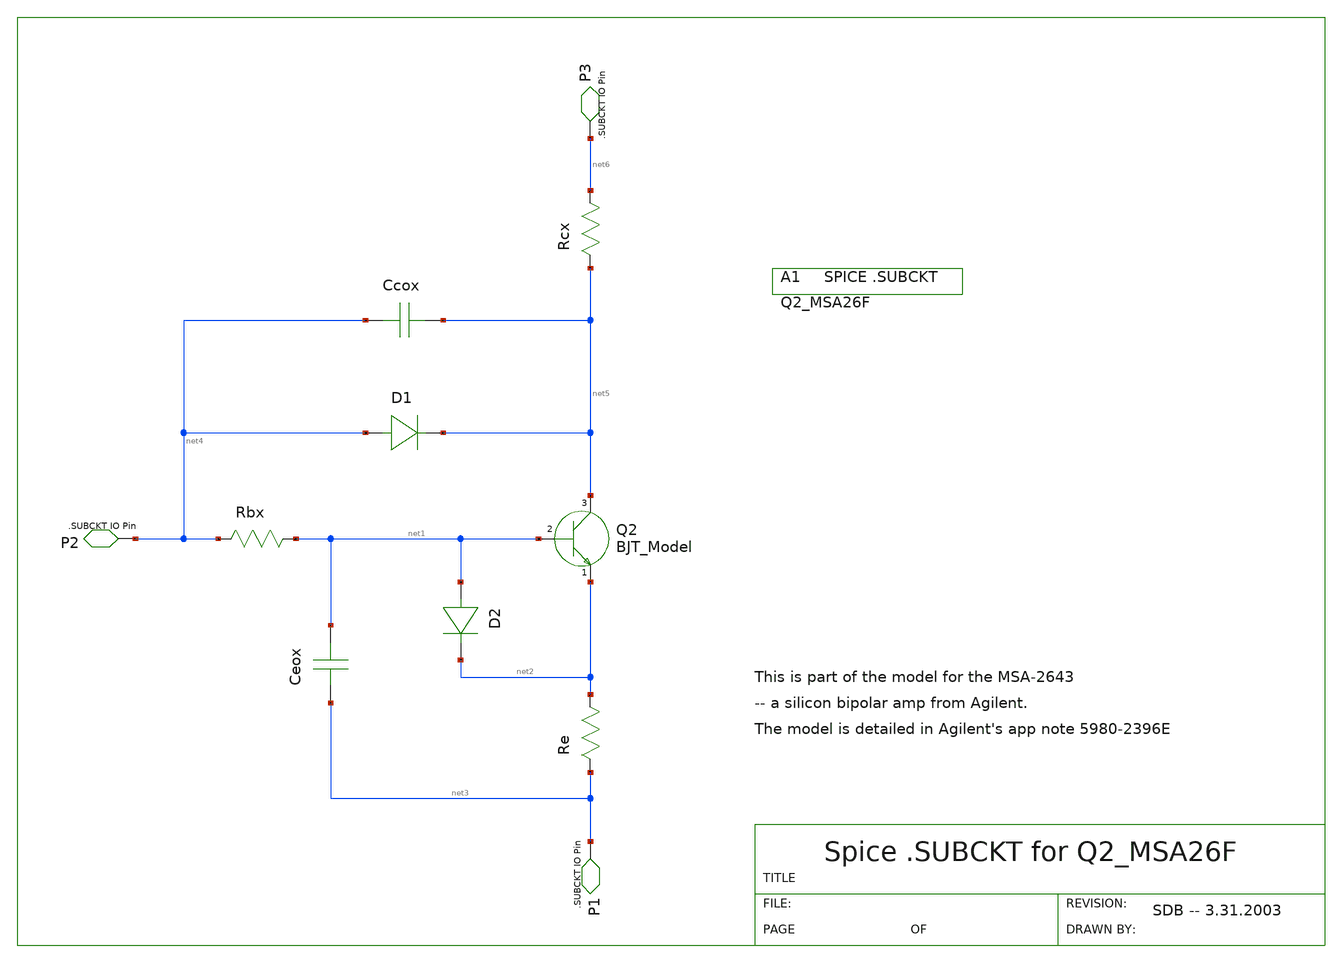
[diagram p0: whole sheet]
** sch_path: xschem_library/gschem_import/Q2.sch
**.subckt Q2
Q2 net5 net2 net1
D1 net4 net5
D2 net1 net2
Ccox net4 net5 6.598e-14F
Ceox net3 net1 2.417e-14F
Rbx net1 net4 0.463
Rcx net6 net5 1.716
Re net2 net3 0.443
P3 net6
P2 net4
P1 net3
A1
**.ends
.end
